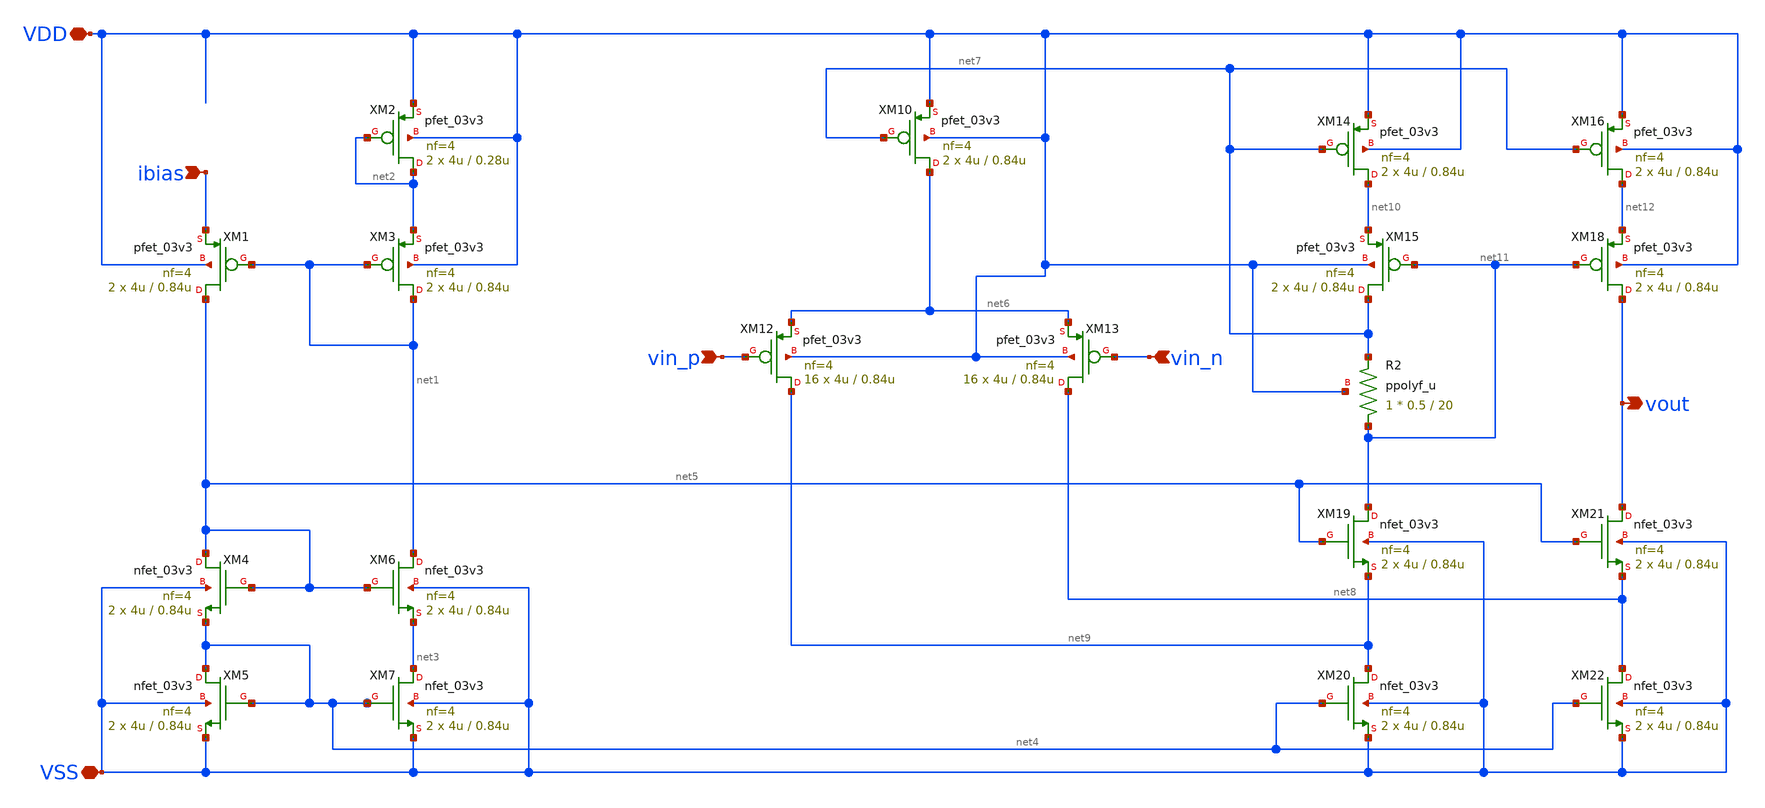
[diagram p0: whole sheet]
** sch_path: xschem/gfmcu_example_amp.sch
**.subckt gfmcu_example_amp vin_n vin_p vout VSS VDD ibias
*.ipin vin_n
*.ipin vin_p
*.opin vout
*.iopin VSS
*.iopin VDD
*.ipin ibias
XM1 net5 net1 ibias VDD pfet_03v3 L=0.84u W=4u nf=4 ad='int((nf+1)/2) * W/nf * 0.18u' as='int((nf+2)/2) * W/nf * 0.18u'
+ pd='2*int((nf+1)/2) * (W/nf + 0.18u)' ps='2*int((nf+2)/2) * (W/nf + 0.18u)' nrd='0.18u / W' nrs='0.18u / W'
+ sa=0 sb=0 sd=0 m=2 par=2
XM2 net2 net2 VDD VDD pfet_03v3 L=0.28u W=4u nf=4 ad='int((nf+1)/2) * W/nf * 0.18u' as='int((nf+2)/2) * W/nf * 0.18u'
+ pd='2*int((nf+1)/2) * (W/nf + 0.18u)' ps='2*int((nf+2)/2) * (W/nf + 0.18u)' nrd='0.18u / W' nrs='0.18u / W'
+ sa=0 sb=0 sd=0 m=2 par=2
XM3 net1 net1 net2 VDD pfet_03v3 L=0.84u W=4u nf=4 ad='int((nf+1)/2) * W/nf * 0.18u' as='int((nf+2)/2) * W/nf * 0.18u'
+ pd='2*int((nf+1)/2) * (W/nf + 0.18u)' ps='2*int((nf+2)/2) * (W/nf + 0.18u)' nrd='0.18u / W' nrs='0.18u / W'
+ sa=0 sb=0 sd=0 m=2 par=2
XM4 net5 net5 net4 VSS nfet_03v3 L=0.84u W=4u nf=4 ad='int((nf+1)/2) * W/nf * 0.18u' as='int((nf+2)/2) * W/nf * 0.18u'
+ pd='2*int((nf+1)/2) * (W/nf + 0.18u)' ps='2*int((nf+2)/2) * (W/nf + 0.18u)' nrd='0.18u / W' nrs='0.18u / W'
+ sa=0 sb=0 sd=0 m=2 par=2
XM5 net4 net4 VSS VSS nfet_03v3 L=0.84u W=4u nf=4 ad='int((nf+1)/2) * W/nf * 0.18u' as='int((nf+2)/2) * W/nf * 0.18u'
+ pd='2*int((nf+1)/2) * (W/nf + 0.18u)' ps='2*int((nf+2)/2) * (W/nf + 0.18u)' nrd='0.18u / W' nrs='0.18u / W'
+ sa=0 sb=0 sd=0 m=2 par=2
XM6 net1 net5 net3 VSS nfet_03v3 L=0.84u W=4u nf=4 ad='int((nf+1)/2) * W/nf * 0.18u' as='int((nf+2)/2) * W/nf * 0.18u'
+ pd='2*int((nf+1)/2) * (W/nf + 0.18u)' ps='2*int((nf+2)/2) * (W/nf + 0.18u)' nrd='0.18u / W' nrs='0.18u / W'
+ sa=0 sb=0 sd=0 m=2 par=2
XM7 net3 net4 VSS VSS nfet_03v3 L=0.84u W=4u nf=4 ad='int((nf+1)/2) * W/nf * 0.18u' as='int((nf+2)/2) * W/nf * 0.18u'
+ pd='2*int((nf+1)/2) * (W/nf + 0.18u)' ps='2*int((nf+2)/2) * (W/nf + 0.18u)' nrd='0.18u / W' nrs='0.18u / W'
+ sa=0 sb=0 sd=0 m=2 par=2
XM10 net6 net7 VDD VDD pfet_03v3 L=0.84u W=4u nf=4 ad='int((nf+1)/2) * W/nf * 0.18u' as='int((nf+2)/2) * W/nf * 0.18u'
+ pd='2*int((nf+1)/2) * (W/nf + 0.18u)' ps='2*int((nf+2)/2) * (W/nf + 0.18u)' nrd='0.18u / W' nrs='0.18u / W'
+ sa=0 sb=0 sd=0 m=2 par=2
XM12 net9 vin_p net6 VDD pfet_03v3 L=0.84u W=4u nf=4 ad='int((nf+1)/2) * W/nf * 0.18u' as='int((nf+2)/2) * W/nf * 0.18u'
+ pd='2*int((nf+1)/2) * (W/nf + 0.18u)' ps='2*int((nf+2)/2) * (W/nf + 0.18u)' nrd='0.18u / W' nrs='0.18u / W'
+ sa=0 sb=0 sd=0 m=16 par=16
XM13 net8 vin_n net6 VDD pfet_03v3 L=0.84u W=4u nf=4 ad='int((nf+1)/2) * W/nf * 0.18u' as='int((nf+2)/2) * W/nf * 0.18u'
+ pd='2*int((nf+1)/2) * (W/nf + 0.18u)' ps='2*int((nf+2)/2) * (W/nf + 0.18u)' nrd='0.18u / W' nrs='0.18u / W'
+ sa=0 sb=0 sd=0 m=16 par=16
XM14 net10 net7 VDD VDD pfet_03v3 L=0.84u W=4u nf=4 ad='int((nf+1)/2) * W/nf * 0.18u' as='int((nf+2)/2) * W/nf * 0.18u'
+ pd='2*int((nf+1)/2) * (W/nf + 0.18u)' ps='2*int((nf+2)/2) * (W/nf + 0.18u)' nrd='0.18u / W' nrs='0.18u / W'
+ sa=0 sb=0 sd=0 m=2 par=2
XM15 net7 net11 net10 VDD pfet_03v3 L=0.84u W=4u nf=4 ad='int((nf+1)/2) * W/nf * 0.18u' as='int((nf+2)/2) * W/nf * 0.18u'
+ pd='2*int((nf+1)/2) * (W/nf + 0.18u)' ps='2*int((nf+2)/2) * (W/nf + 0.18u)' nrd='0.18u / W' nrs='0.18u / W'
+ sa=0 sb=0 sd=0 m=2 par=2
XR2 net11 net7 VDD ppolyf_u r_width=0.5 r_length=20 m=1
XM16 net12 net7 VDD VDD pfet_03v3 L=0.84u W=4u nf=4 ad='int((nf+1)/2) * W/nf * 0.18u' as='int((nf+2)/2) * W/nf * 0.18u'
+ pd='2*int((nf+1)/2) * (W/nf + 0.18u)' ps='2*int((nf+2)/2) * (W/nf + 0.18u)' nrd='0.18u / W' nrs='0.18u / W'
+ sa=0 sb=0 sd=0 m=2 par=2
XM18 vout net11 net12 VDD pfet_03v3 L=0.84u W=4u nf=4 ad='int((nf+1)/2) * W/nf * 0.18u' as='int((nf+2)/2) * W/nf * 0.18u'
+ pd='2*int((nf+1)/2) * (W/nf + 0.18u)' ps='2*int((nf+2)/2) * (W/nf + 0.18u)' nrd='0.18u / W' nrs='0.18u / W'
+ sa=0 sb=0 sd=0 m=2 par=2
XM19 net11 net5 net9 VSS nfet_03v3 L=0.84u W=4u nf=4 ad='int((nf+1)/2) * W/nf * 0.18u' as='int((nf+2)/2) * W/nf * 0.18u'
+ pd='2*int((nf+1)/2) * (W/nf + 0.18u)' ps='2*int((nf+2)/2) * (W/nf + 0.18u)' nrd='0.18u / W' nrs='0.18u / W'
+ sa=0 sb=0 sd=0 m=2 par=2
XM20 net9 net4 VSS VSS nfet_03v3 L=0.84u W=4u nf=4 ad='int((nf+1)/2) * W/nf * 0.18u' as='int((nf+2)/2) * W/nf * 0.18u'
+ pd='2*int((nf+1)/2) * (W/nf + 0.18u)' ps='2*int((nf+2)/2) * (W/nf + 0.18u)' nrd='0.18u / W' nrs='0.18u / W'
+ sa=0 sb=0 sd=0 m=2 par=2
XM21 vout net5 net8 VSS nfet_03v3 L=0.84u W=4u nf=4 ad='int((nf+1)/2) * W/nf * 0.18u' as='int((nf+2)/2) * W/nf * 0.18u'
+ pd='2*int((nf+1)/2) * (W/nf + 0.18u)' ps='2*int((nf+2)/2) * (W/nf + 0.18u)' nrd='0.18u / W' nrs='0.18u / W'
+ sa=0 sb=0 sd=0 m=2 par=2
XM22 net8 net4 VSS VSS nfet_03v3 L=0.84u W=4u nf=4 ad='int((nf+1)/2) * W/nf * 0.18u' as='int((nf+2)/2) * W/nf * 0.18u'
+ pd='2*int((nf+1)/2) * (W/nf + 0.18u)' ps='2*int((nf+2)/2) * (W/nf + 0.18u)' nrd='0.18u / W' nrs='0.18u / W'
+ sa=0 sb=0 sd=0 m=2 par=2
**.ends
.end
